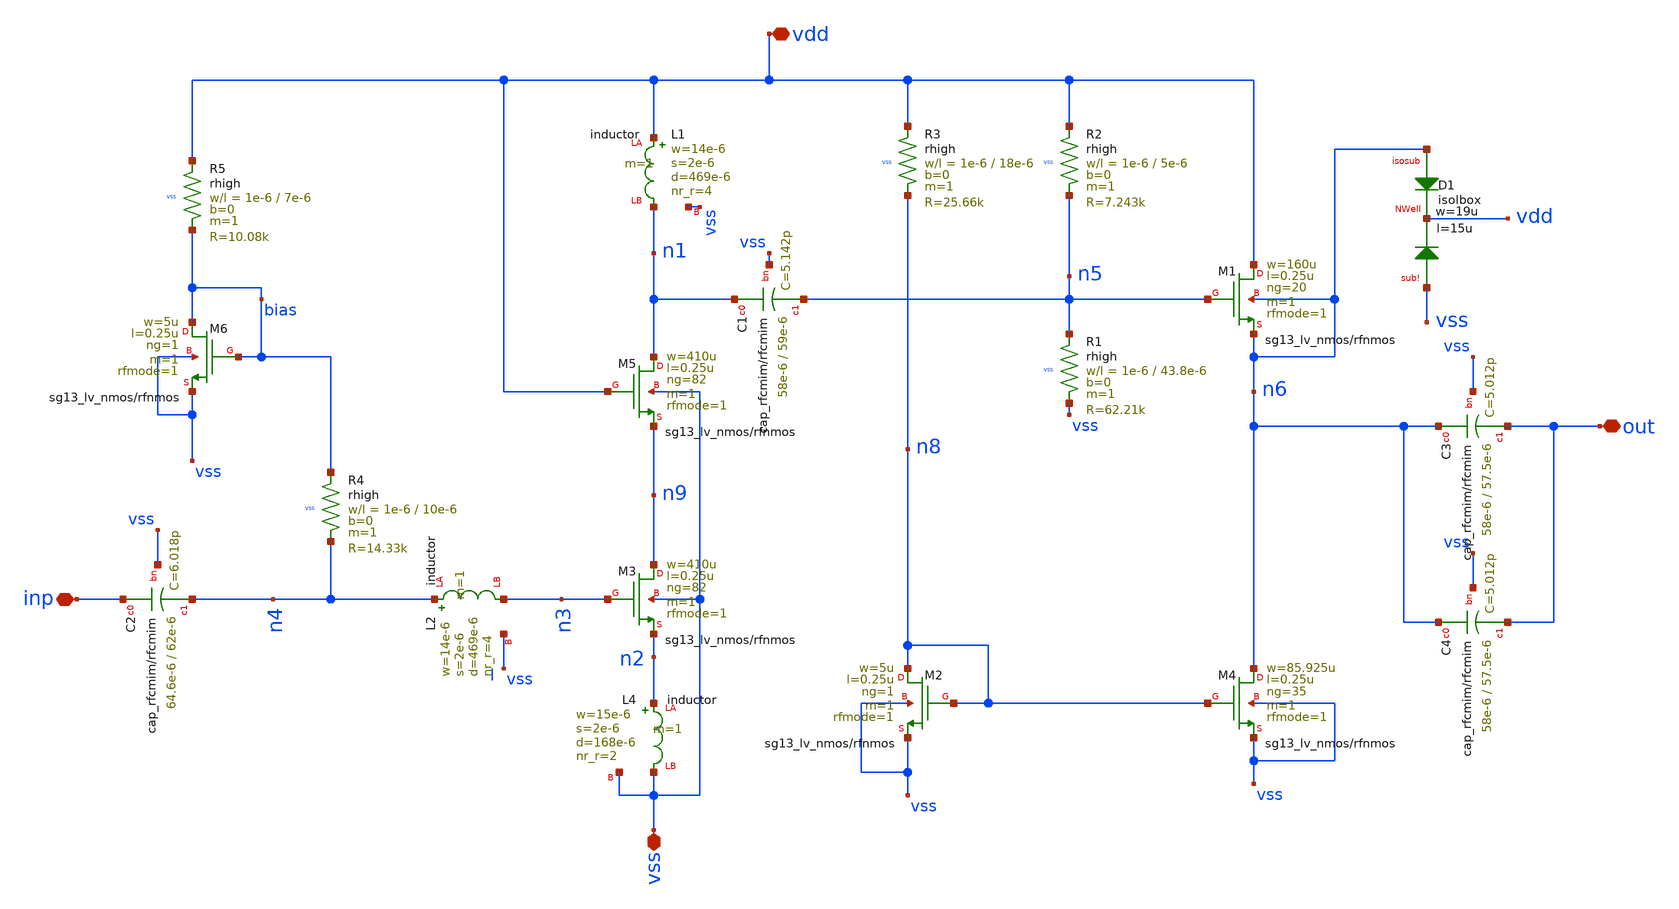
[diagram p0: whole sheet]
** sch_path: LNA7096-main/schematic/xschem/01_lna/LNA_with_buff.sch
**.subckt LNA_with_buff vdd vss inp out
*.iopin vdd
*.iopin vss
*.iopin inp
*.iopin out
XR1 n5 vss vss rhigh w=1e-6 l=43.8e-6 m=1 b=0 mm_ok=1
XR2 vdd n5 vss rhigh w=1e-6 l=5e-6 m=1 b=0 mm_ok=1
XR3 vdd n8 vss rhigh w=1e-6 l=18e-6 m=1 b=0 mm_ok=1
XR4 bias n4 vss rhigh w=1e-6 l=10e-6 m=1 b=0 mm_ok=1
XR5 vdd bias vss rhigh w=1e-6 l=7e-6 m=1 b=0 mm_ok=1
XC1 n1 n5 vss cap_rfcmim w=58e-6 l=59e-6 wfeed=3.0e-6 m=1 mm_ok=1
XC3 n6 out vss cap_rfcmim w=58e-6 l=57.5e-6 wfeed=3.0e-6 m=1 mm_ok=1
XC2 inp n4 vss cap_rfcmim w=64.6e-6 l=62e-6 wfeed=3.0e-6 m=1 mm_ok=1
XC4 n6 out vss cap_rfcmim w=58e-6 l=57.5e-6 wfeed=3.0e-6 m=1 mm_ok=1
XL1 vdd n1 vss inductor w=14e-6 s=2e-6 d=469e-6 nr_r=4 m=1
XL4 n2 vss vss inductor w=15e-6 s=2e-6 d=168e-6 nr_r=2 m=1
XL2 n4 n3 vss inductor w=14e-6 s=2e-6 d=469e-6 nr_r=4 m=1
XM5 n1 vdd n9 vss sg13_lv_nmos w=410u l=0.25u ng=82 m=1 rfmode=1 mm_ok=1
XM3 n9 n3 n2 vss sg13_lv_nmos w=410u l=0.25u ng=82 m=1 rfmode=1 mm_ok=1
XM2 n8 n8 vss vss sg13_lv_nmos w=5u l=0.25u ng=1 m=1 rfmode=1 mm_ok=1
XM4 n6 n8 vss vss sg13_lv_nmos w=85.925u l=0.25u ng=35 m=1 rfmode=1 mm_ok=1
XM1 vdd n5 n6 n6 sg13_lv_nmos w=160u l=0.25u ng=20 m=1 rfmode=1 mm_ok=1
XM6 bias bias vss vss sg13_lv_nmos w=5u l=0.25u ng=1 m=1 rfmode=1 mm_ok=1
XD1 n6 vdd vss isolbox l=15u w=19u
**.ends
.end
